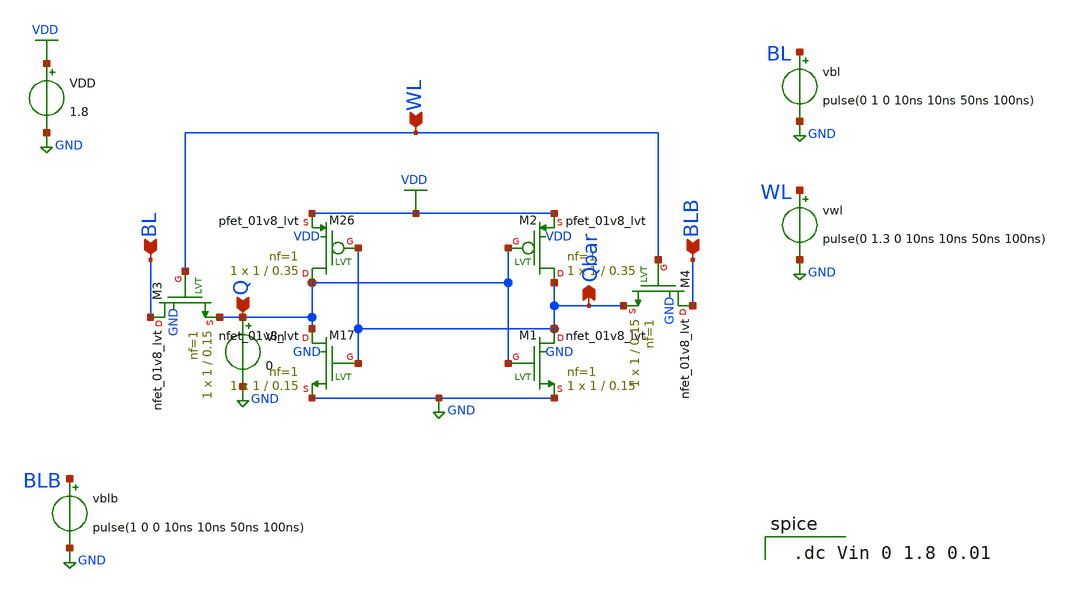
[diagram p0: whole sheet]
** sch_path: sram_6t_cell.sch
**.subckt sram_6t_cell BL WL BLB Q Qbar
*.ipin BL
*.ipin WL
*.ipin BLB
*.ipin Q
*.opin Qbar
XM26 Q Qbar VDD VDD sky130_fd_pr__pfet_01v8_lvt L=0.35 W=1 nf=1 ad='int((1 + 1)/2) * 1 / 1 * 0.29' as='int((1 + 2)/2) * 1 / 1 * 0.29'
+ pd='2*int((1 + 1)/2) * (1 / 1 + 0.29)' ps='2*int((1 + 2)/2) * (1 / 1 + 0.29)' nrd='0.29 / 1 ' nrs='0.29 / 1 '
+ sa=0 sb=0 sd=0 mult=1 m=1
XM17 Q Qbar GND GND sky130_fd_pr__nfet_01v8_lvt L=0.15 W=1 nf=1 ad='int((1 + 1)/2) * 1 / 1 * 0.29' as='int((1 + 2)/2) * 1 / 1 * 0.29'
+ pd='2*int((1 + 1)/2) * (1 / 1 + 0.29)' ps='2*int((1 + 2)/2) * (1 / 1 + 0.29)' nrd='0.29 / 1 ' nrs='0.29 / 1 '
+ sa=0 sb=0 sd=0 mult=1 m=1
XM1 Qbar Q GND GND sky130_fd_pr__nfet_01v8_lvt L=0.15 W=1 nf=1 ad='int((1 + 1)/2) * 1 / 1 * 0.29' as='int((1 + 2)/2) * 1 / 1 * 0.29'
+ pd='2*int((1 + 1)/2) * (1 / 1 + 0.29)' ps='2*int((1 + 2)/2) * (1 / 1 + 0.29)' nrd='0.29 / 1 ' nrs='0.29 / 1 '
+ sa=0 sb=0 sd=0 mult=1 m=1
XM2 Qbar Q VDD VDD sky130_fd_pr__pfet_01v8_lvt L=0.35 W=1 nf=1 ad='int((1 + 1)/2) * 1 / 1 * 0.29' as='int((1 + 2)/2) * 1 / 1 * 0.29'
+ pd='2*int((1 + 1)/2) * (1 / 1 + 0.29)' ps='2*int((1 + 2)/2) * (1 / 1 + 0.29)' nrd='0.29 / 1 ' nrs='0.29 / 1 '
+ sa=0 sb=0 sd=0 mult=1 m=1
VDD VDD GND 1.8
XM3 BL WL Q GND sky130_fd_pr__nfet_01v8_lvt L=0.15 W=1 nf=1 ad='int((1 + 1)/2) * 1 / 1 * 0.29' as='int((1 + 2)/2) * 1 / 1 * 0.29'
+ pd='2*int((1 + 1)/2) * (1 / 1 + 0.29)' ps='2*int((1 + 2)/2) * (1 / 1 + 0.29)' nrd='0.29 / 1 ' nrs='0.29 / 1 '
+ sa=0 sb=0 sd=0 mult=1 m=1
XM4 BLB WL Qbar GND sky130_fd_pr__nfet_01v8_lvt L=0.15 W=1 nf=1 ad='int((1 + 1)/2) * 1 / 1 * 0.29' as='int((1 + 2)/2) * 1 / 1 * 0.29'
+ pd='2*int((1 + 1)/2) * (1 / 1 + 0.29)' ps='2*int((1 + 2)/2) * (1 / 1 + 0.29)' nrd='0.29 / 1 ' nrs='0.29 / 1 '
+ sa=0 sb=0 sd=0 mult=1 m=1
vblb BLB GND pulse(1 0 0 10ns 10ns 50ns 100ns)
vbl BL GND pulse(0 1 0 10ns 10ns 50ns 100ns)
vwl WL GND pulse(0 1.3 0 10ns 10ns 50ns 100ns)
Vin Q GND 0
**** begin user architecture code

** opencircuitdesign pdks install
.lib $::SKYWATER_MODELS/sky130.lib.spice tt



 .dc Vin 0 1.8 0.01

**** end user architecture code
**.ends
.GLOBAL GND
.GLOBAL VDD
.end
